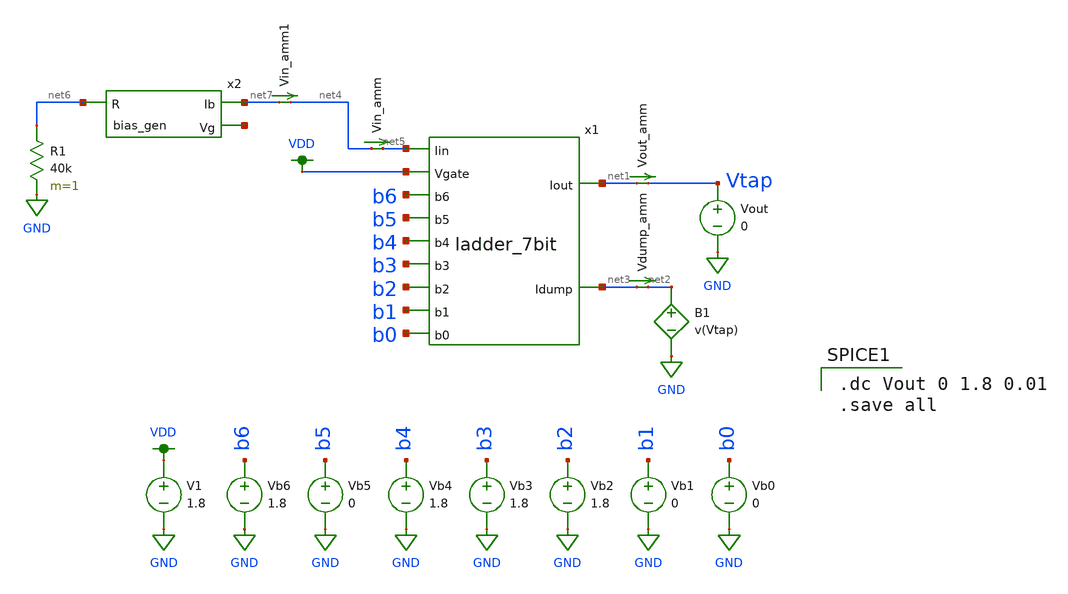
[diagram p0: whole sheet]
** sch_path: test_harness_dcvout.sch
**.subckt test_harness_dcvout
Vb0 b0 GND 0
Vb1 b1 GND 0
Vb2 b2 GND 1.8
Vb3 b3 GND 1.8
Vb4 b4 GND 1.8
Vb5 b5 GND 0
Vb6 b6 GND 1.8
Vout Vtap GND 0
Vout_amm net1 Vtap 0
.save i(vout_amm)
Vdump_amm net3 net2 0
.save i(vdump_amm)
x1 VDD net5 net3 net1 b5 b4 b1 b2 b3 b0 b6 ladder_7bit
Vin_amm net4 net5 0
.save i(vin_amm)
x2 net7 net8 net6 bias_gen
R1 net6 GND 40k m=1
Vin_amm1 net7 net4 0
.save i(vin_amm1)
B1 net2 GND V=v(Vtap)
V1 VDD GND 1.8
**** begin user architecture code

.dc Vout 0 1.8 0.01
.save all


.option wnflag=1
.param MC_SWITCH=0.0
.lib ~/skywater/skywater-pdk/libraries/sky130_fd_pr_ngspice/latest/models/sky130.lib.spice tt

**** end user architecture code
**.ends
.GLOBAL GND
.GLOBAL VDD
.end
